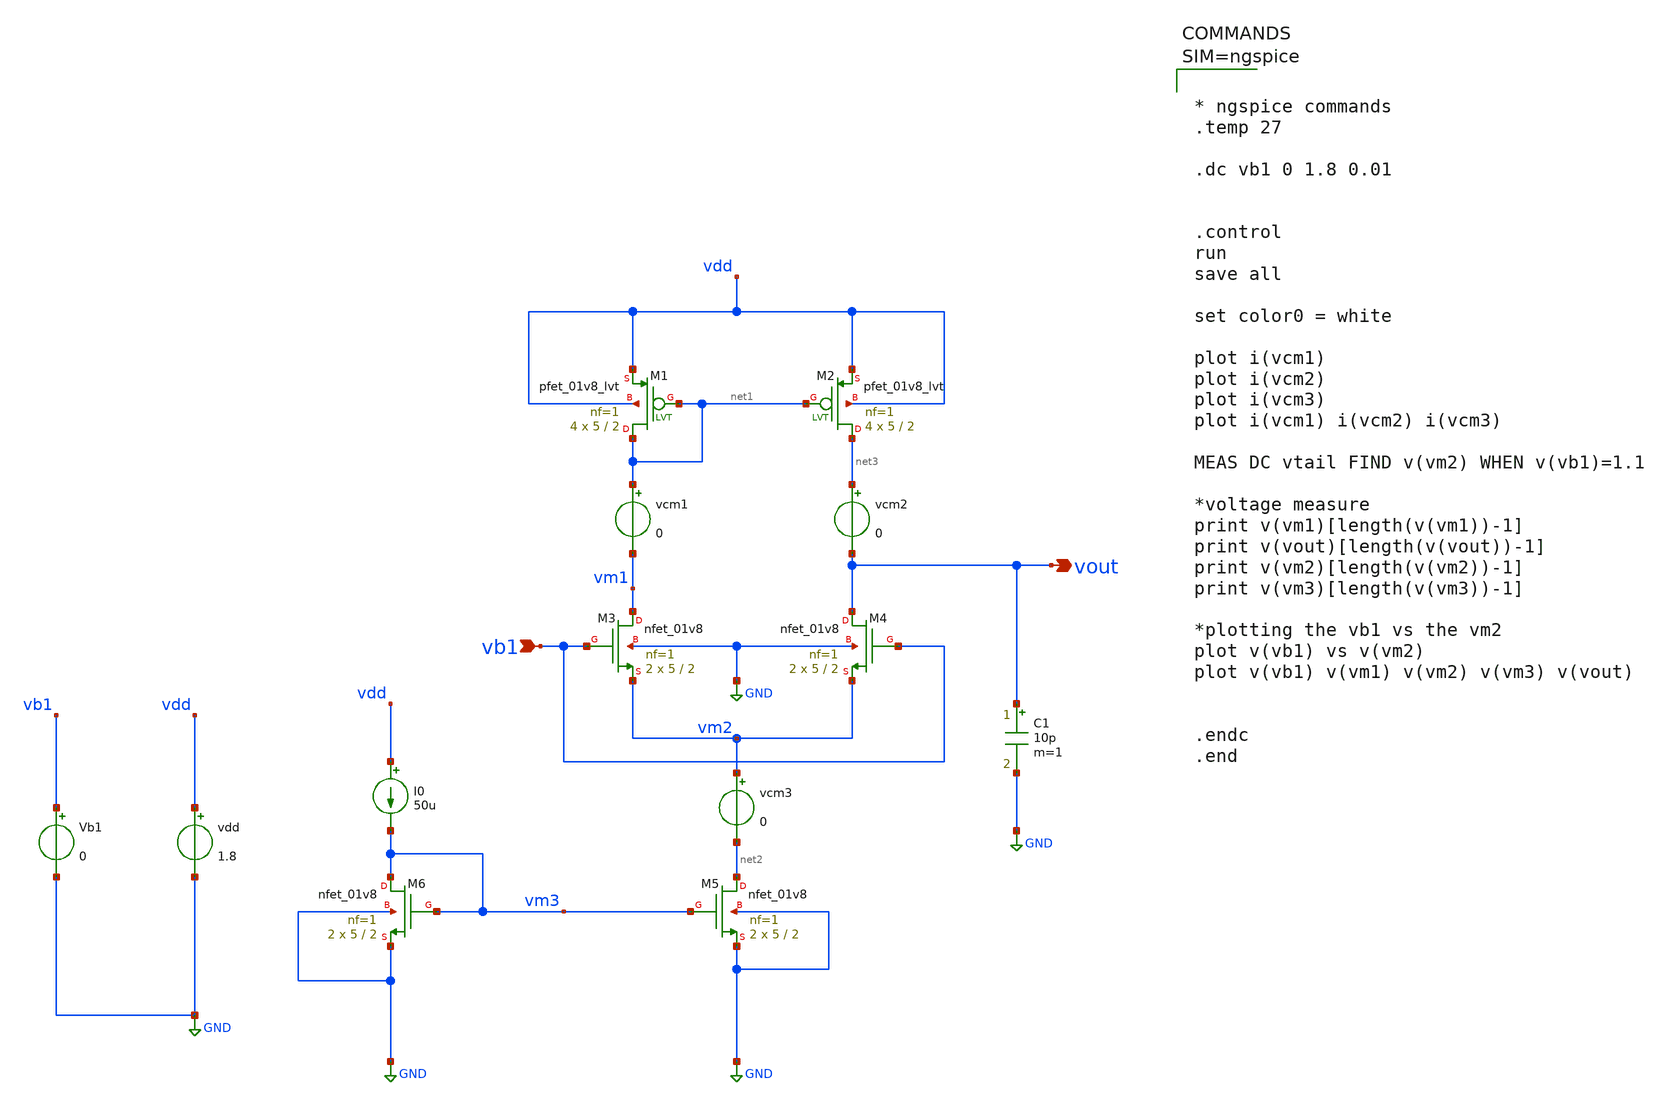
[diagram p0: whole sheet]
** sch_path: testbenches/Differential_Amplifier_parameter_Extraction.sch
**.subckt Differential_Amplifier_parameter_Extraction vout vb1
*.opin vout
*.ipin vb1
XM5 net2 vm3 GND GND sky130_fd_pr__nfet_01v8 L=2 W=5 nf=1 ad='int((1 + 1)/2) * 5 / 1 * 0.29' as='int((1 + 2)/2) * 5 / 1 * 0.29'
+ pd='2*int((1 + 1)/2) * (5 / 1 + 0.29)' ps='2*int((1 + 2)/2) * (5 / 1 + 0.29)' nrd='0.29 / 5 ' nrs='0.29 / 5 '
+ sa=0 sb=0 sd=0 mult=2 m=2
I0 vdd vm3 50u
vdd vdd GND 1.8
Vb1 vb1 GND 0
XM2 net3 net1 vdd vdd sky130_fd_pr__pfet_01v8_lvt L=2 W=5 nf=1 ad='int((1 + 1)/2) * 5 / 1 * 0.29' as='int((1 + 2)/2) * 5 / 1 * 0.29'
+ pd='2*int((1 + 1)/2) * (5 / 1 + 0.29)' ps='2*int((1 + 2)/2) * (5 / 1 + 0.29)' nrd='0.29 / 5 ' nrs='0.29 / 5 '
+ sa=0 sb=0 sd=0 mult=4 m=4
XM3 vm1 vb1 vm2 GND sky130_fd_pr__nfet_01v8 L=2 W=5 nf=1 ad='int((1 + 1)/2) * 5 / 1 * 0.29' as='int((1 + 2)/2) * 5 / 1 * 0.29'
+ pd='2*int((1 + 1)/2) * (5 / 1 + 0.29)' ps='2*int((1 + 2)/2) * (5 / 1 + 0.29)' nrd='0.29 / 5 ' nrs='0.29 / 5 '
+ sa=0 sb=0 sd=0 mult=2 m=2
XM4 vout vb1 vm2 GND sky130_fd_pr__nfet_01v8 L=2 W=5 nf=1 ad='int((1 + 1)/2) * 5 / 1 * 0.29' as='int((1 + 2)/2) * 5 / 1 * 0.29'
+ pd='2*int((1 + 1)/2) * (5 / 1 + 0.29)' ps='2*int((1 + 2)/2) * (5 / 1 + 0.29)' nrd='0.29 / 5 ' nrs='0.29 / 5 '
+ sa=0 sb=0 sd=0 mult=2 m=2
XM6 vm3 vm3 GND GND sky130_fd_pr__nfet_01v8 L=2 W=5 nf=1 ad='int((1 + 1)/2) * 5 / 1 * 0.29' as='int((1 + 2)/2) * 5 / 1 * 0.29'
+ pd='2*int((1 + 1)/2) * (5 / 1 + 0.29)' ps='2*int((1 + 2)/2) * (5 / 1 + 0.29)' nrd='0.29 / 5 ' nrs='0.29 / 5 '
+ sa=0 sb=0 sd=0 mult=2 m=2
XM1 net1 net1 vdd vdd sky130_fd_pr__pfet_01v8_lvt L=2 W=5 nf=1 ad='int((1 + 1)/2) * 5 / 1 * 0.29' as='int((1 + 2)/2) * 5 / 1 * 0.29'
+ pd='2*int((1 + 1)/2) * (5 / 1 + 0.29)' ps='2*int((1 + 2)/2) * (5 / 1 + 0.29)' nrd='0.29 / 5 ' nrs='0.29 / 5 '
+ sa=0 sb=0 sd=0 mult=4 m=4
vcm3 vm2 net2 0
vcm1 net1 vm1 0
vcm2 net3 vout 0
C1 vout GND 10p m=1
**** begin user architecture code

** opencircuitdesign pdks install
.lib $::SKYWATER_MODELS/sky130.lib.spice tt




* ngspice commands
.temp 27

.dc vb1 0 1.8 0.01


.control
run
save all

set color0 = white

plot i(vcm1)
plot i(vcm2)
plot i(vcm3)
plot i(vcm1) i(vcm2) i(vcm3)

MEAS DC vtail FIND v(vm2) WHEN v(vb1)=1.1

*voltage measure
print v(vm1)[length(v(vm1))-1]
print v(vout)[length(v(vout))-1]
print v(vm2)[length(v(vm2))-1]
print v(vm3)[length(v(vm3))-1]

*plotting the vb1 vs the vm2
plot v(vb1) vs v(vm2)
plot v(vb1) v(vm1) v(vm2) v(vm3) v(vout)


.endc
.end



**** end user architecture code
**.ends
.GLOBAL GND
.end
